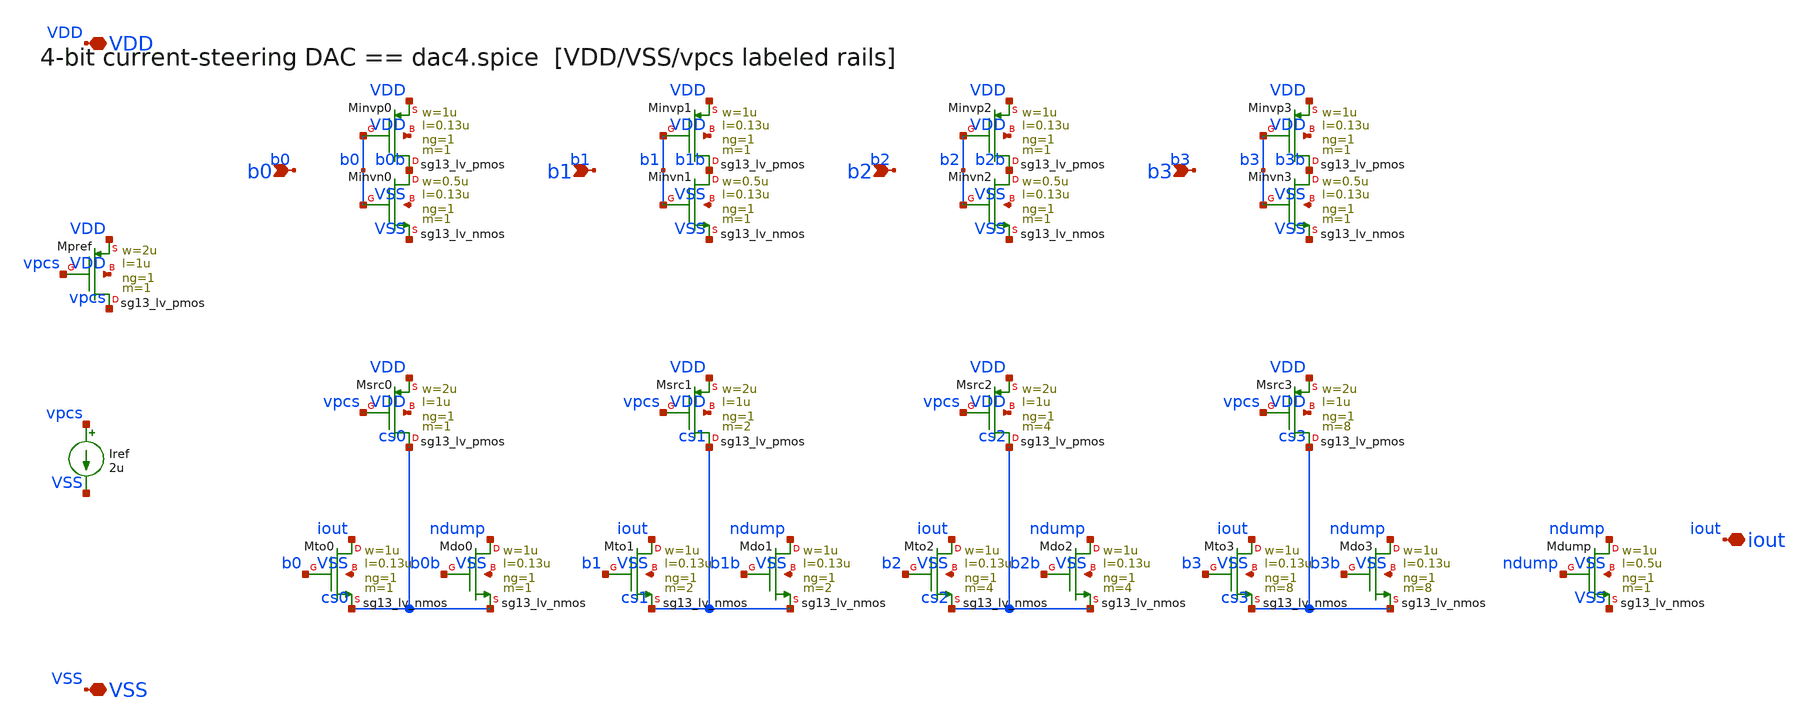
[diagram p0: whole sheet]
** sch_path: macros/dac/schematic/xschem/dac4.sch
**.subckt dac4 b0 b1 b2 b3 iout VDD VSS
*.ipin b0
*.ipin b1
*.ipin b2
*.ipin b3
*.iopin iout
*.iopin VDD
*.iopin VSS
XMpref vpcs vpcs VDD VDD sg13_lv_pmos w=2u l=1u ng=1 m=1 mm_ok=1
Iref vpcs VSS 2u
XMinvp0 b0b b0 VDD VDD sg13_lv_pmos w=1u l=0.13u ng=1 m=1 mm_ok=1
XMinvn0 b0b b0 VSS VSS sg13_lv_nmos w=0.5u l=0.13u ng=1 m=1 mm_ok=1
XMsrc0 cs0 vpcs VDD VDD sg13_lv_pmos w=2u l=1u ng=1 m=1 mm_ok=1
XMto0 iout b0 cs0 VSS sg13_lv_nmos w=1u l=0.13u ng=1 m=1 mm_ok=1
XMdo0 ndump b0b cs0 VSS sg13_lv_nmos w=1u l=0.13u ng=1 m=1 mm_ok=1
XMinvp1 b1b b1 VDD VDD sg13_lv_pmos w=1u l=0.13u ng=1 m=1 mm_ok=1
XMinvn1 b1b b1 VSS VSS sg13_lv_nmos w=0.5u l=0.13u ng=1 m=1 mm_ok=1
XMsrc1 cs1 vpcs VDD VDD sg13_lv_pmos w=2u l=1u ng=1 m=2 mm_ok=1
XMto1 iout b1 cs1 VSS sg13_lv_nmos w=1u l=0.13u ng=1 m=2 mm_ok=1
XMdo1 ndump b1b cs1 VSS sg13_lv_nmos w=1u l=0.13u ng=1 m=2 mm_ok=1
XMinvp2 b2b b2 VDD VDD sg13_lv_pmos w=1u l=0.13u ng=1 m=1 mm_ok=1
XMinvn2 b2b b2 VSS VSS sg13_lv_nmos w=0.5u l=0.13u ng=1 m=1 mm_ok=1
XMsrc2 cs2 vpcs VDD VDD sg13_lv_pmos w=2u l=1u ng=1 m=4 mm_ok=1
XMto2 iout b2 cs2 VSS sg13_lv_nmos w=1u l=0.13u ng=1 m=4 mm_ok=1
XMdo2 ndump b2b cs2 VSS sg13_lv_nmos w=1u l=0.13u ng=1 m=4 mm_ok=1
XMinvp3 b3b b3 VDD VDD sg13_lv_pmos w=1u l=0.13u ng=1 m=1 mm_ok=1
XMinvn3 b3b b3 VSS VSS sg13_lv_nmos w=0.5u l=0.13u ng=1 m=1 mm_ok=1
XMsrc3 cs3 vpcs VDD VDD sg13_lv_pmos w=2u l=1u ng=1 m=8 mm_ok=1
XMto3 iout b3 cs3 VSS sg13_lv_nmos w=1u l=0.13u ng=1 m=8 mm_ok=1
XMdo3 ndump b3b cs3 VSS sg13_lv_nmos w=1u l=0.13u ng=1 m=8 mm_ok=1
XMdump ndump ndump VSS VSS sg13_lv_nmos w=1u l=0.5u ng=1 m=1 mm_ok=1
**.ends
.end
